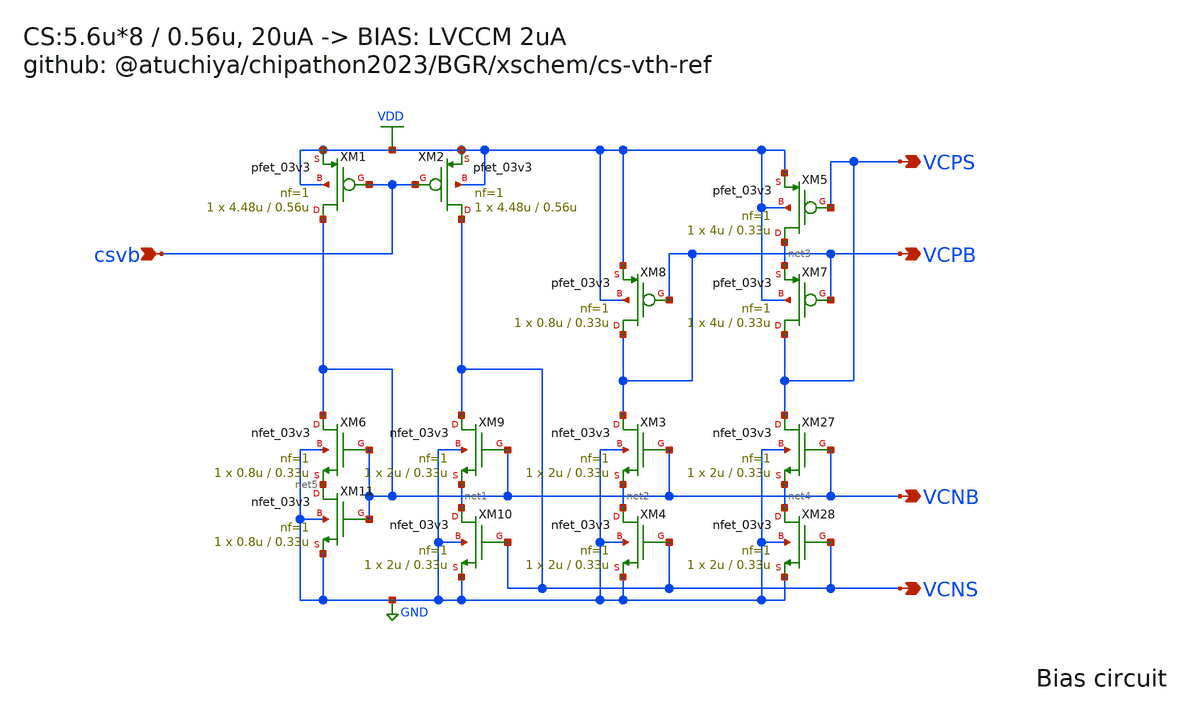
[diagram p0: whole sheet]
** sch_path: schematic/csbias.sch
**.subckt csbias VCPS VCPB VCNB VCNS csvb
*.opin VCPS
*.opin VCPB
*.opin VCNB
*.opin VCNS
*.ipin csvb
XM1 VCNB csvb VDD VDD pfet_03v3 L=0.56u W=4.48u nf=1 ad='int((nf+1)/2) * W/nf * 0.18u' as='int((nf+2)/2) * W/nf * 0.18u'
+ pd='2*int((nf+1)/2) * (W/nf + 0.18u)' ps='2*int((nf+2)/2) * (W/nf + 0.18u)' nrd='0.18u / W' nrs='0.18u / W'
+ sa=0 sb=0 sd=0 m=1
XM2 VCNS csvb VDD VDD pfet_03v3 L=0.56u W=4.48u nf=1 ad='int((nf+1)/2) * W/nf * 0.18u' as='int((nf+2)/2) * W/nf * 0.18u'
+ pd='2*int((nf+1)/2) * (W/nf + 0.18u)' ps='2*int((nf+2)/2) * (W/nf + 0.18u)' nrd='0.18u / W' nrs='0.18u / W'
+ sa=0 sb=0 sd=0 m=1
XM9 VCNS VCNB net1 GND nfet_03v3 L=0.33u W=2u nf=1 ad='int((nf+1)/2) * W/nf * 0.18u' as='int((nf+2)/2) * W/nf * 0.18u'
+ pd='2*int((nf+1)/2) * (W/nf + 0.18u)' ps='2*int((nf+2)/2) * (W/nf + 0.18u)' nrd='0.18u / W' nrs='0.18u / W'
+ sa=0 sb=0 sd=0 m=1
XM10 net1 VCNS GND GND nfet_03v3 L=0.33u W=2u nf=1 ad='int((nf+1)/2) * W/nf * 0.18u' as='int((nf+2)/2) * W/nf * 0.18u'
+ pd='2*int((nf+1)/2) * (W/nf + 0.18u)' ps='2*int((nf+2)/2) * (W/nf + 0.18u)' nrd='0.18u / W' nrs='0.18u / W'
+ sa=0 sb=0 sd=0 m=1
XM6 VCNB VCNB net5 GND nfet_03v3 L=0.33u W=0.8u nf=1 ad='int((nf+1)/2) * W/nf * 0.18u' as='int((nf+2)/2) * W/nf * 0.18u'
+ pd='2*int((nf+1)/2) * (W/nf + 0.18u)' ps='2*int((nf+2)/2) * (W/nf + 0.18u)' nrd='0.18u / W' nrs='0.18u / W'
+ sa=0 sb=0 sd=0 m=1
XM3 VCPB VCNB net2 GND nfet_03v3 L=0.33u W=2u nf=1 ad='int((nf+1)/2) * W/nf * 0.18u' as='int((nf+2)/2) * W/nf * 0.18u'
+ pd='2*int((nf+1)/2) * (W/nf + 0.18u)' ps='2*int((nf+2)/2) * (W/nf + 0.18u)' nrd='0.18u / W' nrs='0.18u / W'
+ sa=0 sb=0 sd=0 m=1
XM4 net2 VCNS GND GND nfet_03v3 L=0.33u W=2u nf=1 ad='int((nf+1)/2) * W/nf * 0.18u' as='int((nf+2)/2) * W/nf * 0.18u'
+ pd='2*int((nf+1)/2) * (W/nf + 0.18u)' ps='2*int((nf+2)/2) * (W/nf + 0.18u)' nrd='0.18u / W' nrs='0.18u / W'
+ sa=0 sb=0 sd=0 m=1
XM5 net3 VCPS VDD VDD pfet_03v3 L=0.33u W=4u nf=1 ad='int((nf+1)/2) * W/nf * 0.18u' as='int((nf+2)/2) * W/nf * 0.18u'
+ pd='2*int((nf+1)/2) * (W/nf + 0.18u)' ps='2*int((nf+2)/2) * (W/nf + 0.18u)' nrd='0.18u / W' nrs='0.18u / W'
+ sa=0 sb=0 sd=0 m=1
XM7 VCPS VCPB net3 VDD pfet_03v3 L=0.33u W=4u nf=1 ad='int((nf+1)/2) * W/nf * 0.18u' as='int((nf+2)/2) * W/nf * 0.18u'
+ pd='2*int((nf+1)/2) * (W/nf + 0.18u)' ps='2*int((nf+2)/2) * (W/nf + 0.18u)' nrd='0.18u / W' nrs='0.18u / W'
+ sa=0 sb=0 sd=0 m=1
XM8 VCPB VCPB VDD VDD pfet_03v3 L=0.33u W=0.8u nf=1 ad='int((nf+1)/2) * W/nf * 0.18u' as='int((nf+2)/2) * W/nf * 0.18u'
+ pd='2*int((nf+1)/2) * (W/nf + 0.18u)' ps='2*int((nf+2)/2) * (W/nf + 0.18u)' nrd='0.18u / W' nrs='0.18u / W'
+ sa=0 sb=0 sd=0 m=1
XM27 VCPS VCNB net4 GND nfet_03v3 L=0.33u W=2u nf=1 ad='int((nf+1)/2) * W/nf * 0.18u' as='int((nf+2)/2) * W/nf * 0.18u'
+ pd='2*int((nf+1)/2) * (W/nf + 0.18u)' ps='2*int((nf+2)/2) * (W/nf + 0.18u)' nrd='0.18u / W' nrs='0.18u / W'
+ sa=0 sb=0 sd=0 m=1
XM28 net4 VCNS GND GND nfet_03v3 L=0.33u W=2u nf=1 ad='int((nf+1)/2) * W/nf * 0.18u' as='int((nf+2)/2) * W/nf * 0.18u'
+ pd='2*int((nf+1)/2) * (W/nf + 0.18u)' ps='2*int((nf+2)/2) * (W/nf + 0.18u)' nrd='0.18u / W' nrs='0.18u / W'
+ sa=0 sb=0 sd=0 m=1
XM11 net5 VCNB GND GND nfet_03v3 L=0.33u W=0.8u nf=1 ad='int((nf+1)/2) * W/nf * 0.18u' as='int((nf+2)/2) * W/nf * 0.18u'
+ pd='2*int((nf+1)/2) * (W/nf + 0.18u)' ps='2*int((nf+2)/2) * (W/nf + 0.18u)' nrd='0.18u / W' nrs='0.18u / W'
+ sa=0 sb=0 sd=0 m=1
**.ends
.GLOBAL VDD
.GLOBAL GND
.end
